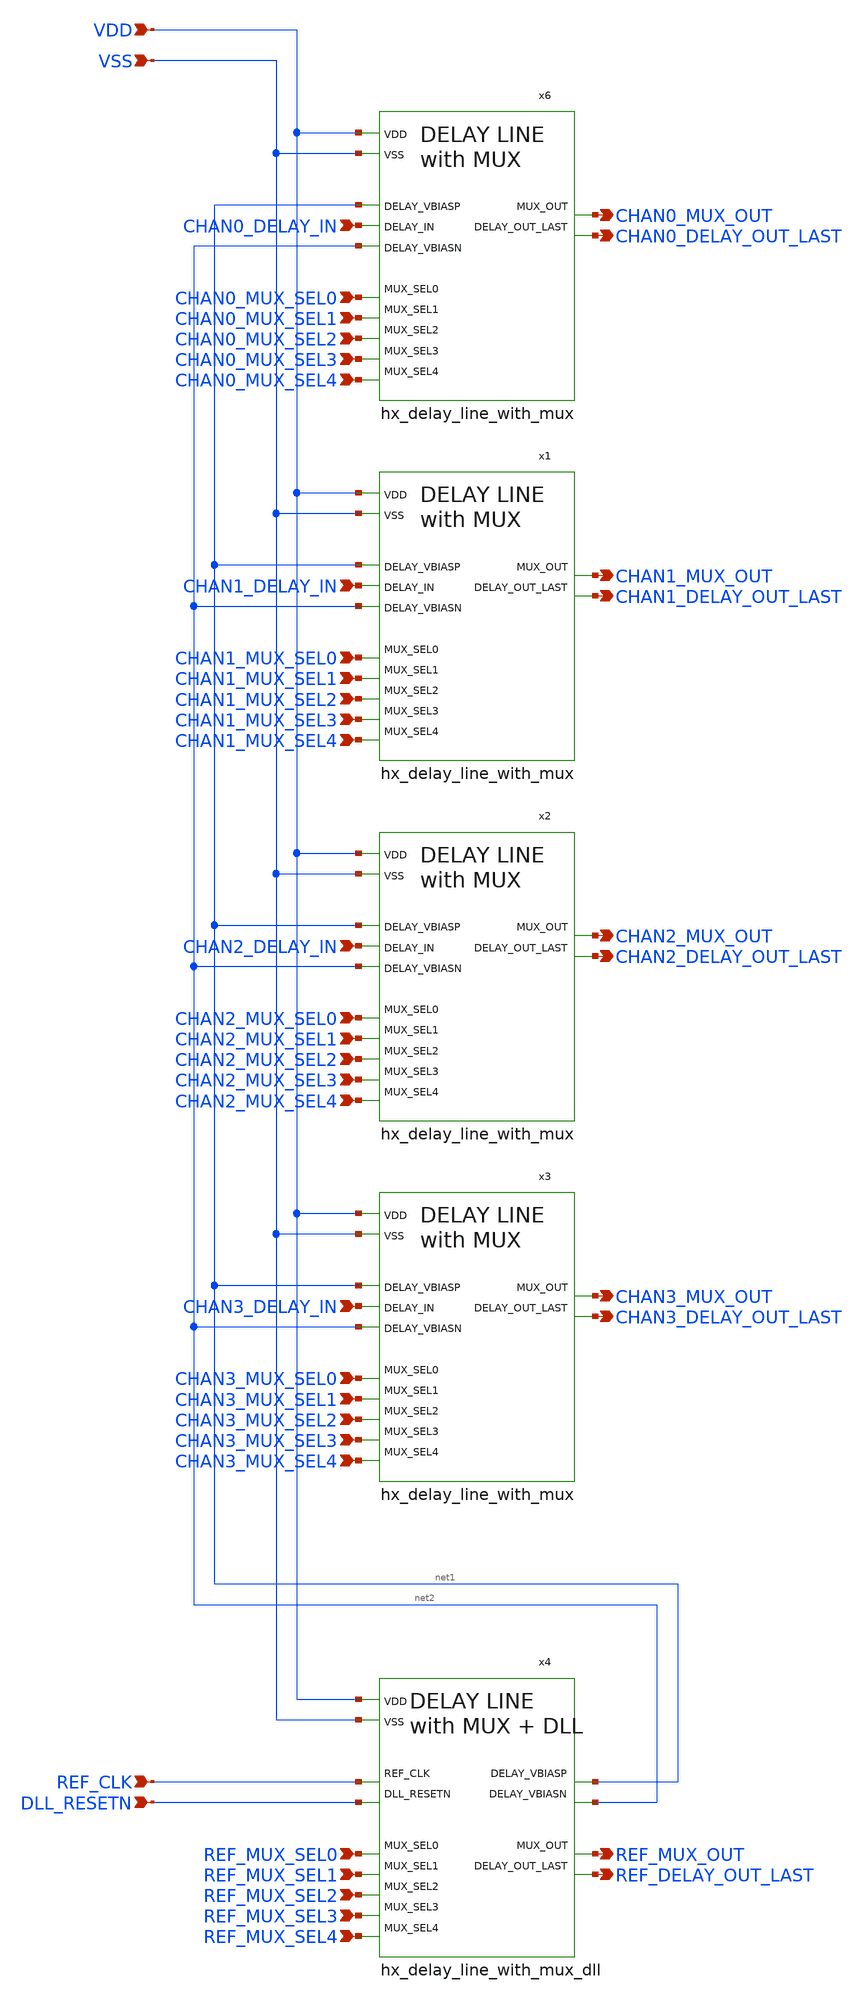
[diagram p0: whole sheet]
** sch_path: schematics/hx_delay_bank.sch
**.subckt hx_delay_bank VDD VSS REF_CLK DLL_RESETN REF_MUX_SEL0 REF_MUX_SEL1 REF_MUX_SEL2
*+ REF_MUX_SEL3 REF_MUX_SEL4 CHAN3_MUX_SEL0 CHAN3_MUX_SEL1 CHAN3_MUX_SEL2 CHAN3_MUX_SEL3 CHAN3_MUX_SEL4
*+ CHAN2_MUX_SEL0 CHAN2_MUX_SEL1 CHAN2_MUX_SEL2 CHAN2_MUX_SEL3 CHAN2_MUX_SEL4 CHAN1_MUX_SEL0 CHAN1_MUX_SEL1
*+ CHAN1_MUX_SEL2 CHAN1_MUX_SEL3 CHAN1_MUX_SEL4 CHAN0_MUX_SEL0 CHAN0_MUX_SEL1 CHAN0_MUX_SEL2 CHAN0_MUX_SEL3
*+ CHAN0_MUX_SEL4 CHAN3_DELAY_IN CHAN2_DELAY_IN CHAN1_DELAY_IN CHAN0_DELAY_IN CHAN0_MUX_OUT CHAN0_DELAY_OUT_LAST
*+ CHAN1_MUX_OUT CHAN1_DELAY_OUT_LAST CHAN2_MUX_OUT CHAN2_DELAY_OUT_LAST CHAN3_MUX_OUT CHAN3_DELAY_OUT_LAST
*+ REF_MUX_OUT REF_DELAY_OUT_LAST
*.ipin VDD
*.ipin VSS
*.ipin REF_CLK
*.ipin DLL_RESETN
*.ipin REF_MUX_SEL0
*.ipin REF_MUX_SEL1
*.ipin REF_MUX_SEL2
*.ipin REF_MUX_SEL3
*.ipin REF_MUX_SEL4
*.ipin CHAN3_MUX_SEL0
*.ipin CHAN3_MUX_SEL1
*.ipin CHAN3_MUX_SEL2
*.ipin CHAN3_MUX_SEL3
*.ipin CHAN3_MUX_SEL4
*.ipin CHAN2_MUX_SEL0
*.ipin CHAN2_MUX_SEL1
*.ipin CHAN2_MUX_SEL2
*.ipin CHAN2_MUX_SEL3
*.ipin CHAN2_MUX_SEL4
*.ipin CHAN1_MUX_SEL0
*.ipin CHAN1_MUX_SEL1
*.ipin CHAN1_MUX_SEL2
*.ipin CHAN1_MUX_SEL3
*.ipin CHAN1_MUX_SEL4
*.ipin CHAN0_MUX_SEL0
*.ipin CHAN0_MUX_SEL1
*.ipin CHAN0_MUX_SEL2
*.ipin CHAN0_MUX_SEL3
*.ipin CHAN0_MUX_SEL4
*.ipin CHAN3_DELAY_IN
*.ipin CHAN2_DELAY_IN
*.ipin CHAN1_DELAY_IN
*.ipin CHAN0_DELAY_IN
*.opin CHAN0_MUX_OUT
*.opin CHAN0_DELAY_OUT_LAST
*.opin CHAN1_MUX_OUT
*.opin CHAN1_DELAY_OUT_LAST
*.opin CHAN2_MUX_OUT
*.opin CHAN2_DELAY_OUT_LAST
*.opin CHAN3_MUX_OUT
*.opin CHAN3_DELAY_OUT_LAST
*.opin REF_MUX_OUT
*.opin REF_DELAY_OUT_LAST
x1 CHAN1_DELAY_OUT_LAST VSS VDD CHAN1_DELAY_IN CHAN1_MUX_SEL0 CHAN1_MUX_SEL1 CHAN1_MUX_OUT
+ CHAN1_MUX_SEL4 CHAN1_MUX_SEL2 CHAN1_MUX_SEL3 net2 net1 hx_delay_line_with_mux
x2 CHAN2_DELAY_OUT_LAST VSS VDD CHAN2_DELAY_IN CHAN2_MUX_SEL0 CHAN2_MUX_SEL1 CHAN2_MUX_OUT
+ CHAN2_MUX_SEL4 CHAN2_MUX_SEL2 CHAN2_MUX_SEL3 net2 net1 hx_delay_line_with_mux
x3 CHAN3_DELAY_OUT_LAST VSS VDD CHAN3_DELAY_IN CHAN3_MUX_SEL0 CHAN3_MUX_SEL1 CHAN3_MUX_OUT
+ CHAN3_MUX_SEL4 CHAN3_MUX_SEL2 CHAN3_MUX_SEL3 net2 net1 hx_delay_line_with_mux
x6 CHAN0_DELAY_OUT_LAST VSS VDD CHAN0_DELAY_IN CHAN0_MUX_SEL0 CHAN0_MUX_SEL1 CHAN0_MUX_OUT
+ CHAN0_MUX_SEL4 CHAN0_MUX_SEL2 CHAN0_MUX_SEL3 net2 net1 hx_delay_line_with_mux
x4 VDD REF_DELAY_OUT_LAST VSS net2 net1 REF_CLK DLL_RESETN REF_MUX_SEL0 REF_MUX_SEL1 REF_MUX_OUT
+ REF_MUX_SEL4 REF_MUX_SEL2 REF_MUX_SEL3 hx_delay_line_with_mux_dll
**.ends
.end
